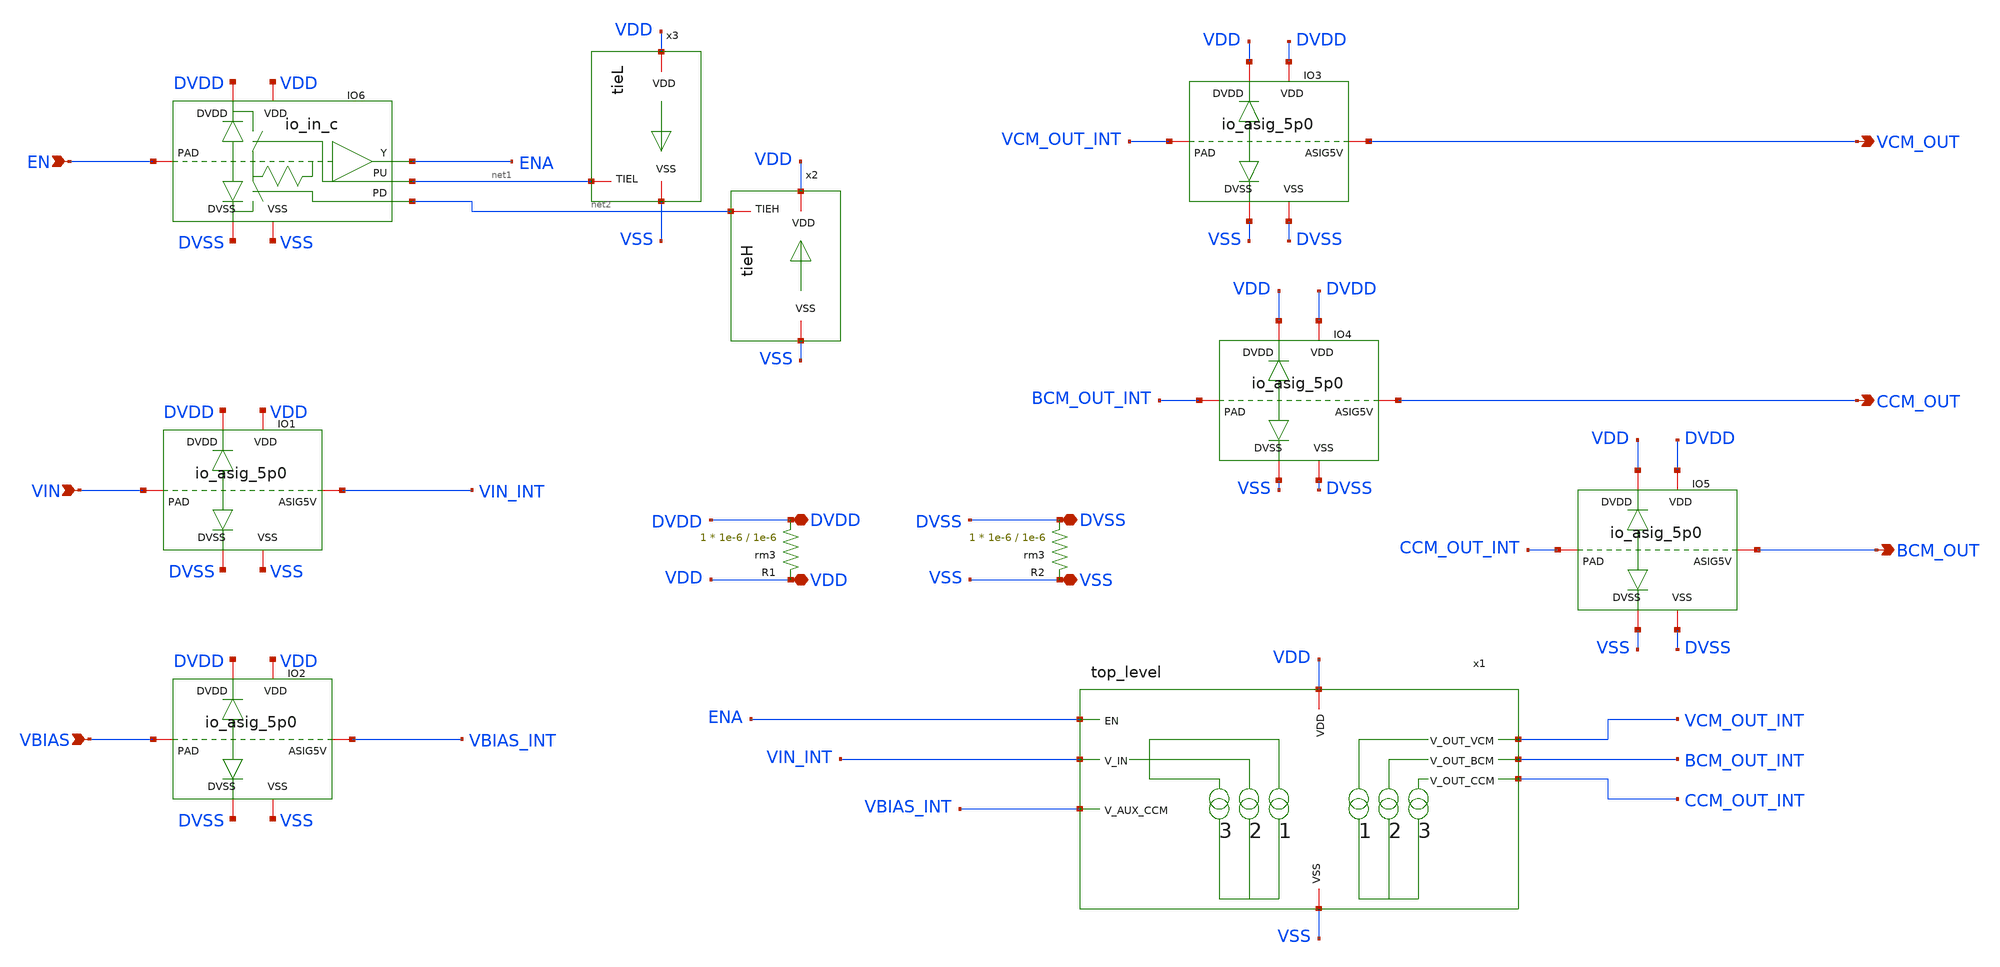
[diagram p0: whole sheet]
** sch_path: blocks/composite/regulated_cascoded_cmirror/xschem/int_top_tb.sch
**.subckt int_top_tb EN VDD DVDD DVSS VSS VIN VBIAS VCM_OUT BCM_OUT CCM_OUT
*.ipin EN
*.iopin VDD
*.iopin DVDD
*.iopin DVSS
*.iopin VSS
*.ipin VIN
*.ipin VBIAS
*.opin VCM_OUT
*.opin BCM_OUT
*.opin CCM_OUT
x1 VDD ENA VIN_INT VCM_OUT_INT BCM_OUT_INT CCM_OUT_INT VBIAS_INT VSS top_level
XR1 DVDD VDD rm3 r_width=1e-6 r_length=1e-6 m=1
XR2 DVSS VSS rm3 r_width=1e-6 r_length=1e-6 m=1
XIO6 DVDD DVSS EN net2 net1 VDD VSS ENA gf180mcu_fd_io__in_c
x2 net2 VDD VSS tieH
x3 VDD net1 VSS tieL
XIO1 DVSS DVDD VSS VDD VIN VIN_INT gf180mcu_fd_io__asig_5p0_extracted
XIO2 DVSS DVDD VSS VDD VBIAS VBIAS_INT gf180mcu_fd_io__asig_5p0_extracted
XIO3 VSS VDD DVSS DVDD VCM_OUT_INT VCM_OUT gf180mcu_fd_io__asig_5p0_extracted
XIO4 VSS VDD DVSS DVDD BCM_OUT_INT CCM_OUT gf180mcu_fd_io__asig_5p0_extracted
XIO5 VSS VDD DVSS DVDD CCM_OUT_INT BCM_OUT gf180mcu_fd_io__asig_5p0_extracted
**.ends
.end
